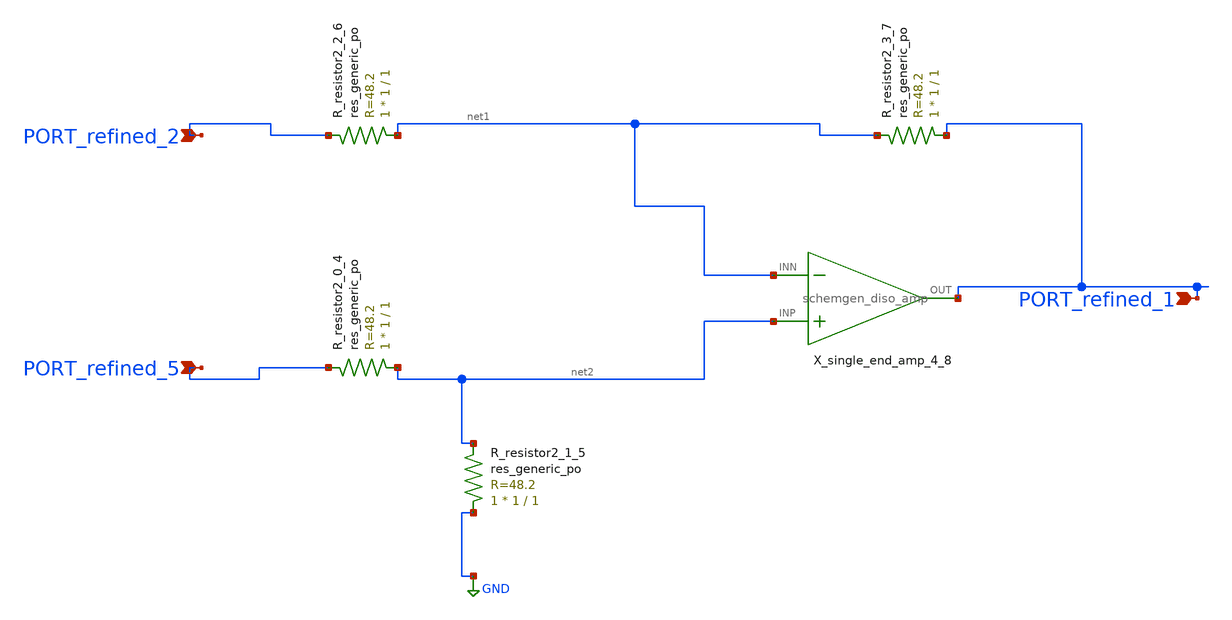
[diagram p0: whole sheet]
** sch_path: schematics/Image2Net/012.sch
**.subckt 012 PORT_refined_1 PORT_refined_5 PORT_refined_2
*.ipin PORT_refined_1
*.ipin PORT_refined_5
*.ipin PORT_refined_2
XR_resistor2_0_4 net2 PORT_refined_5 sky130_fd_pr__res_generic_po W=1 L=1 m=1
XR_resistor2_1_5 GND net2 sky130_fd_pr__res_generic_po W=1 L=1 m=1
XR_resistor2_2_6 net1 PORT_refined_2 sky130_fd_pr__res_generic_po W=1 L=1 m=1
XR_resistor2_3_7 PORT_refined_1 net1 sky130_fd_pr__res_generic_po W=1 L=1 m=1
X_single_end_amp_4_8 net2 net1 PORT_refined_1 schemgen_diso_amp
**.ends

* expanding   symbol:  schemgen_diso_amp.sym # of pins=3
** sym_path: symbols/schemgen_diso_amp.sym
.subckt schemgen_diso_amp INP INN OUT
* SchemGen ideal op-amp: Vout = 1e5 * (V(INP) - V(INN))
E1 OUT 0 INP INN 1e5
.ends schemgen_diso_amp
.GLOBAL GND
.end
